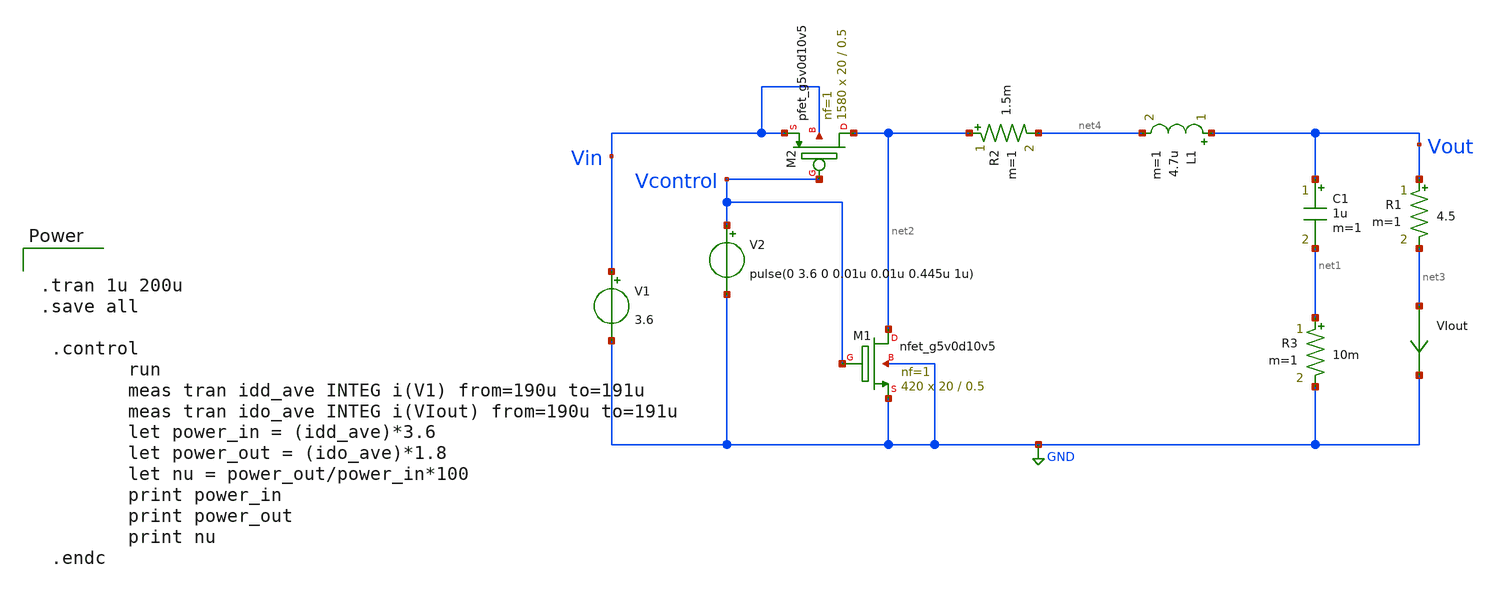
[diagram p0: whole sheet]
** sch_path: Abishek_Sam_group/Buck_converter.sch
**.subckt Buck_converter
XM1 net2 Vcontrol GND GND sky130_fd_pr__nfet_g5v0d10v5 L=0.5 W=20 nf=1 ad='int((nf+1)/2) * W/nf * 0.29'
+ as='int((nf+2)/2) * W/nf * 0.29' pd='2*int((nf+1)/2) * (W/nf + 0.29)' ps='2*int((nf+2)/2) * (W/nf + 0.29)'
+ nrd='0.29 / W' nrs='0.29 / W' sa=0 sb=0 sd=0 mult=420 m=420
XM2 net2 Vcontrol Vin Vin sky130_fd_pr__pfet_g5v0d10v5 L=0.5 W=20 nf=1 ad='int((nf+1)/2) * W/nf * 0.29'
+ as='int((nf+2)/2) * W/nf * 0.29' pd='2*int((nf+1)/2) * (W/nf + 0.29)' ps='2*int((nf+2)/2) * (W/nf + 0.29)'
+ nrd='0.29 / W' nrs='0.29 / W' sa=0 sb=0 sd=0 mult=1580 m=1580
C1 Vout net1 1u m=1
L1 Vout net4 4.7u m=1
R1 Vout net3 4.5 m=1
V1 Vin GND 3.6
R2 net2 net4 1.5m m=1
R3 net1 GND 10m m=1
V2 Vcontrol GND pulse(0 3.6 0 0.01u 0.01u 0.445u 1u)
VIout net3 GND 0
.save i(viout)
**** begin user architecture code

.lib $::SKYWATER_MODELS/sky130.lib.spice tt

**** end user architecture code
**.ends
.GLOBAL GND
**** begin user architecture code


.tran 1u 200u
.save all

 .control
        run
        meas tran idd_ave INTEG i(V1) from=190u to=191u
        meas tran ido_ave INTEG i(VIout) from=190u to=191u
        let power_in = (idd_ave)*3.6
        let power_out = (ido_ave)*1.8
        let nu = power_out/power_in*100
        print power_in
        print power_out
        print nu
 .endc


**** end user architecture code
.end
